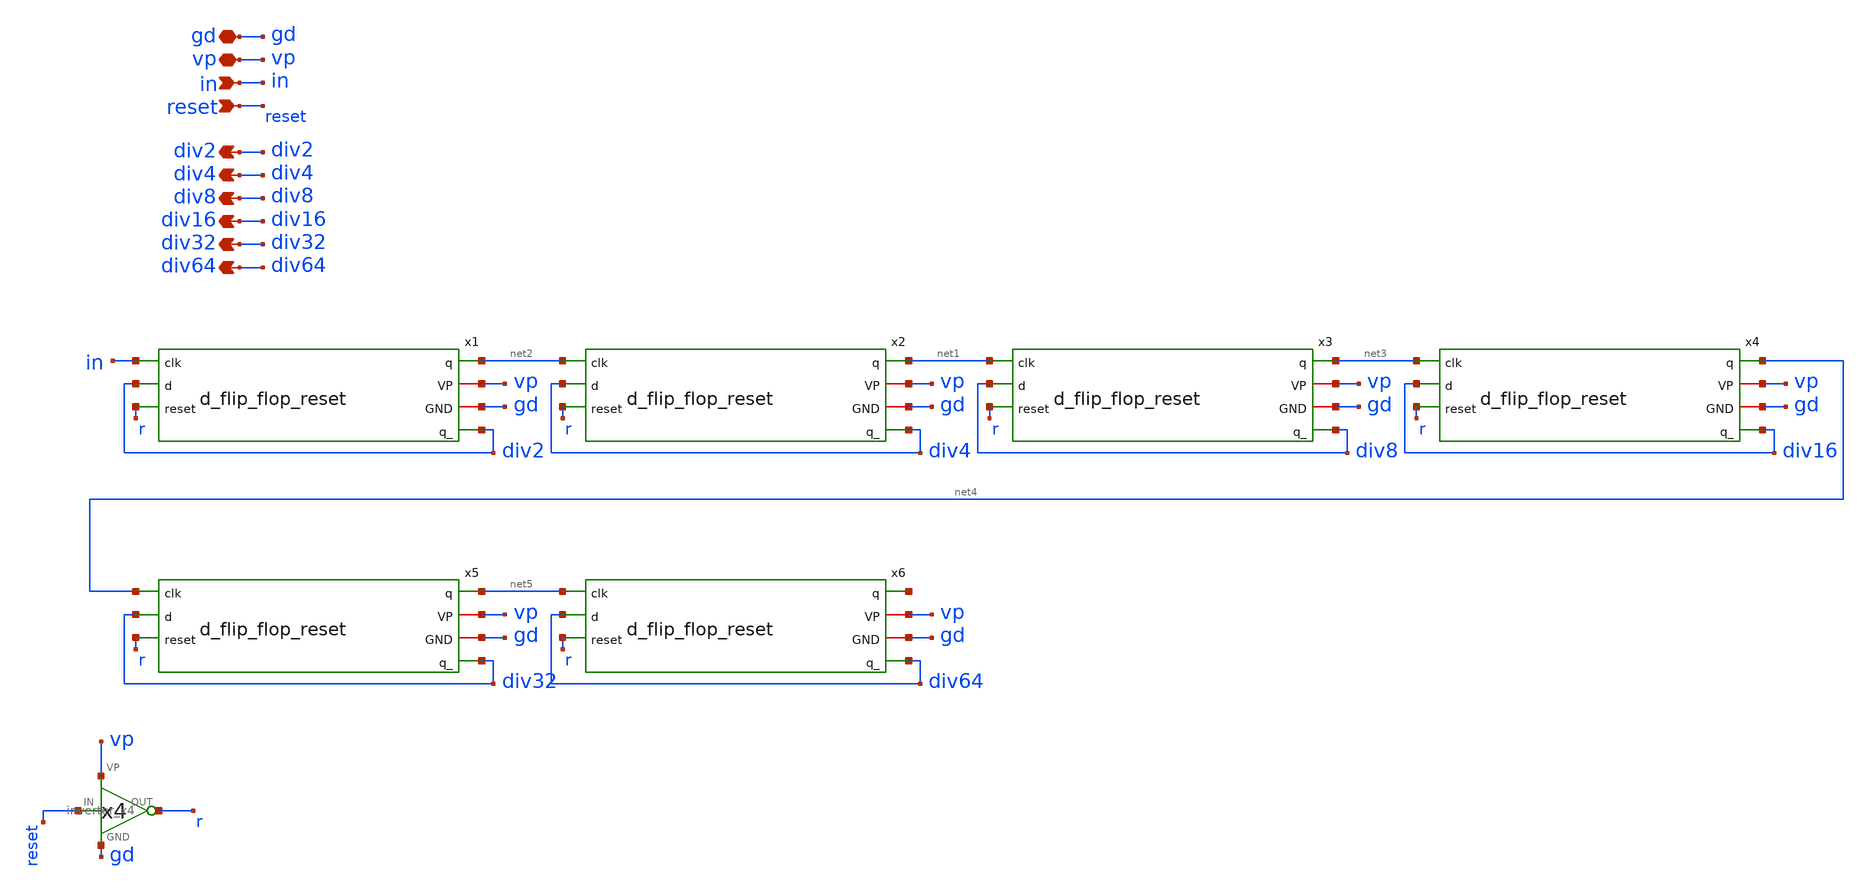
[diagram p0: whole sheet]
** sch_path: divider/schematics/div_with_reset.sch
**.subckt div_with_reset gd in vp div2 div4 div8 div16 div32 div64 reset
*.iopin gd
*.ipin in
*.iopin vp
*.opin div2
*.opin div4
*.opin div8
*.opin div16
*.opin div32
*.opin div64
*.ipin reset
x7 reset r vp gd inverter_x4
x1 net2 vp gd div2 in div2 r d_flip_flop_reset
x2 net1 vp gd div4 net2 div4 r d_flip_flop_reset
x3 net3 vp gd div8 net1 div8 r d_flip_flop_reset
x4 net4 vp gd div16 net3 div16 r d_flip_flop_reset
x5 net5 vp gd div32 net4 div32 r d_flip_flop_reset
x6 net6 vp gd div64 net5 div64 r d_flip_flop_reset
**.ends
.end
